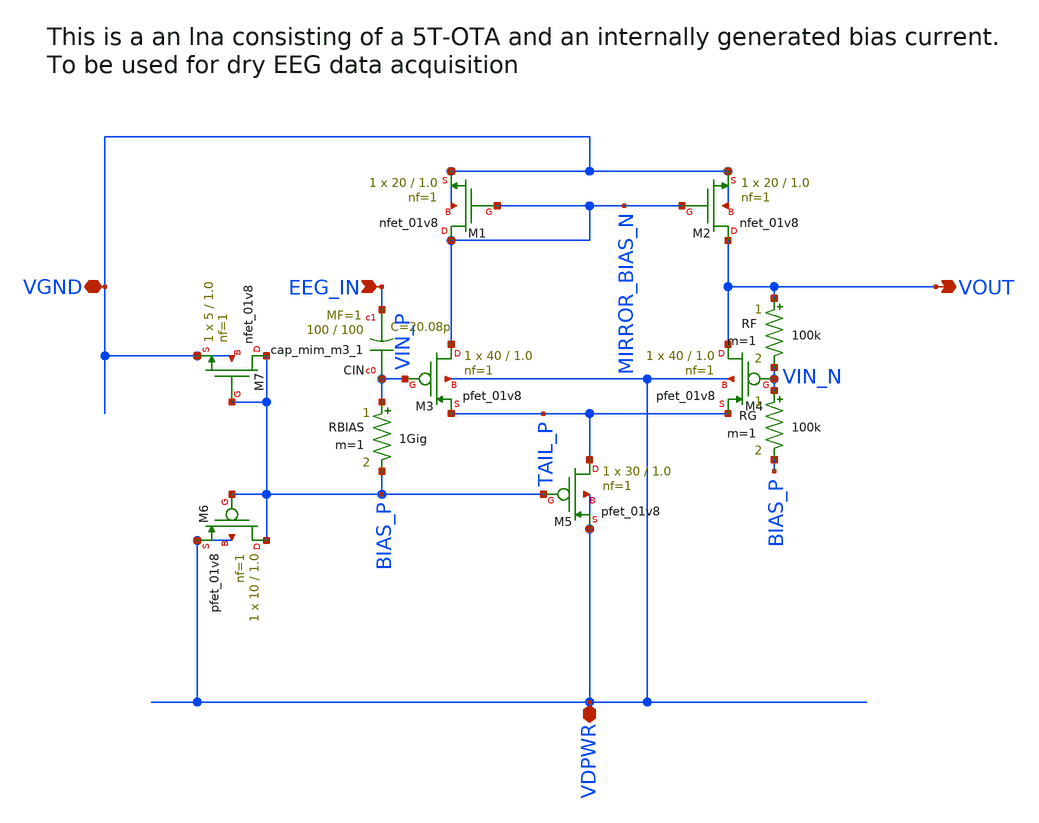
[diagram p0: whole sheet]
** sch_path: xschem/eeg_lna.sch
**.subckt eeg_lna VGND EEG_IN VDPWR VOUT
*.iopin VGND
*.ipin EEG_IN
*.iopin VDPWR
*.opin VOUT
XM1 MIRROR_BIAS_N MIRROR_BIAS_N VGND VGND sky130_fd_pr__nfet_01v8 L=1.0 W=20 nf=1 ad='int((1 + 1)/2) * 20 / 1 * 0.29'
+ as='int((1 + 2)/2) * 20 / 1 * 0.29' pd='2*int((1 + 1)/2) * (20 / 1 + 0.29)' ps='2*int((1 + 2)/2) * (20 / 1 + 0.29)'
+ nrd='0.29 / 20 ' nrs='0.29 / 20 ' sa=0 sb=0 sd=0 mult=1 m=1
XM2 VOUT MIRROR_BIAS_N VGND VGND sky130_fd_pr__nfet_01v8 L=1.0 W=20 nf=1 ad='int((1 + 1)/2) * 20 / 1 * 0.29'
+ as='int((1 + 2)/2) * 20 / 1 * 0.29' pd='2*int((1 + 1)/2) * (20 / 1 + 0.29)' ps='2*int((1 + 2)/2) * (20 / 1 + 0.29)'
+ nrd='0.29 / 20 ' nrs='0.29 / 20 ' sa=0 sb=0 sd=0 mult=1 m=1
XM3 MIRROR_BIAS_N VIN_P TAIL_P VDPWR sky130_fd_pr__pfet_01v8 L=1.0 W=40 nf=1 ad='int((1 + 1)/2) * 40 / 1 * 0.29'
+ as='int((1 + 2)/2) * 40 / 1 * 0.29' pd='2*int((1 + 1)/2) * (40 / 1 + 0.29)' ps='2*int((1 + 2)/2) * (40 / 1 + 0.29)'
+ nrd='0.29 / 40 ' nrs='0.29 / 40 ' sa=0 sb=0 sd=0 mult=1 m=1
XM4 VOUT VIN_N TAIL_P VDPWR sky130_fd_pr__pfet_01v8 L=1.0 W=40 nf=1 ad='int((1 + 1)/2) * 40 / 1 * 0.29'
+ as='int((1 + 2)/2) * 40 / 1 * 0.29' pd='2*int((1 + 1)/2) * (40 / 1 + 0.29)' ps='2*int((1 + 2)/2) * (40 / 1 + 0.29)'
+ nrd='0.29 / 40 ' nrs='0.29 / 40 ' sa=0 sb=0 sd=0 mult=1 m=1
XM5 TAIL_P BIAS_P VDPWR VDPWR sky130_fd_pr__pfet_01v8 L=1.0 W=30 nf=1 ad='int((1 + 1)/2) * 30 / 1 * 0.29'
+ as='int((1 + 2)/2) * 30 / 1 * 0.29' pd='2*int((1 + 1)/2) * (30 / 1 + 0.29)' ps='2*int((1 + 2)/2) * (30 / 1 + 0.29)'
+ nrd='0.29 / 30 ' nrs='0.29 / 30 ' sa=0 sb=0 sd=0 mult=1 m=1
XM6 BIAS_P BIAS_P VDPWR VDPWR sky130_fd_pr__pfet_01v8 L=1.0 W=10 nf=1 ad='int((1 + 1)/2) * 10 / 1 * 0.29'
+ as='int((1 + 2)/2) * 10 / 1 * 0.29' pd='2*int((1 + 1)/2) * (10 / 1 + 0.29)' ps='2*int((1 + 2)/2) * (10 / 1 + 0.29)'
+ nrd='0.29 / 10 ' nrs='0.29 / 10 ' sa=0 sb=0 sd=0 mult=1 m=1
XM7 BIAS_P BIAS_P VGND VGND sky130_fd_pr__nfet_01v8 L=1.0 W=5 nf=1 ad='int((1 + 1)/2) * 5 / 1 * 0.29'
+ as='int((1 + 2)/2) * 5 / 1 * 0.29' pd='2*int((1 + 1)/2) * (5 / 1 + 0.29)' ps='2*int((1 + 2)/2) * (5 / 1 + 0.29)'
+ nrd='0.29 / 5 ' nrs='0.29 / 5 ' sa=0 sb=0 sd=0 mult=1 m=1
XCIN VIN_P EEG_IN sky130_fd_pr__cap_mim_m3_1 W=100 L=100 MF=1 m=1
RBIAS VIN_P BIAS_P 1Gig m=1
RF VOUT VIN_N 100k m=1
RG VIN_N BIAS_P 100k m=1
**.ends
.end
